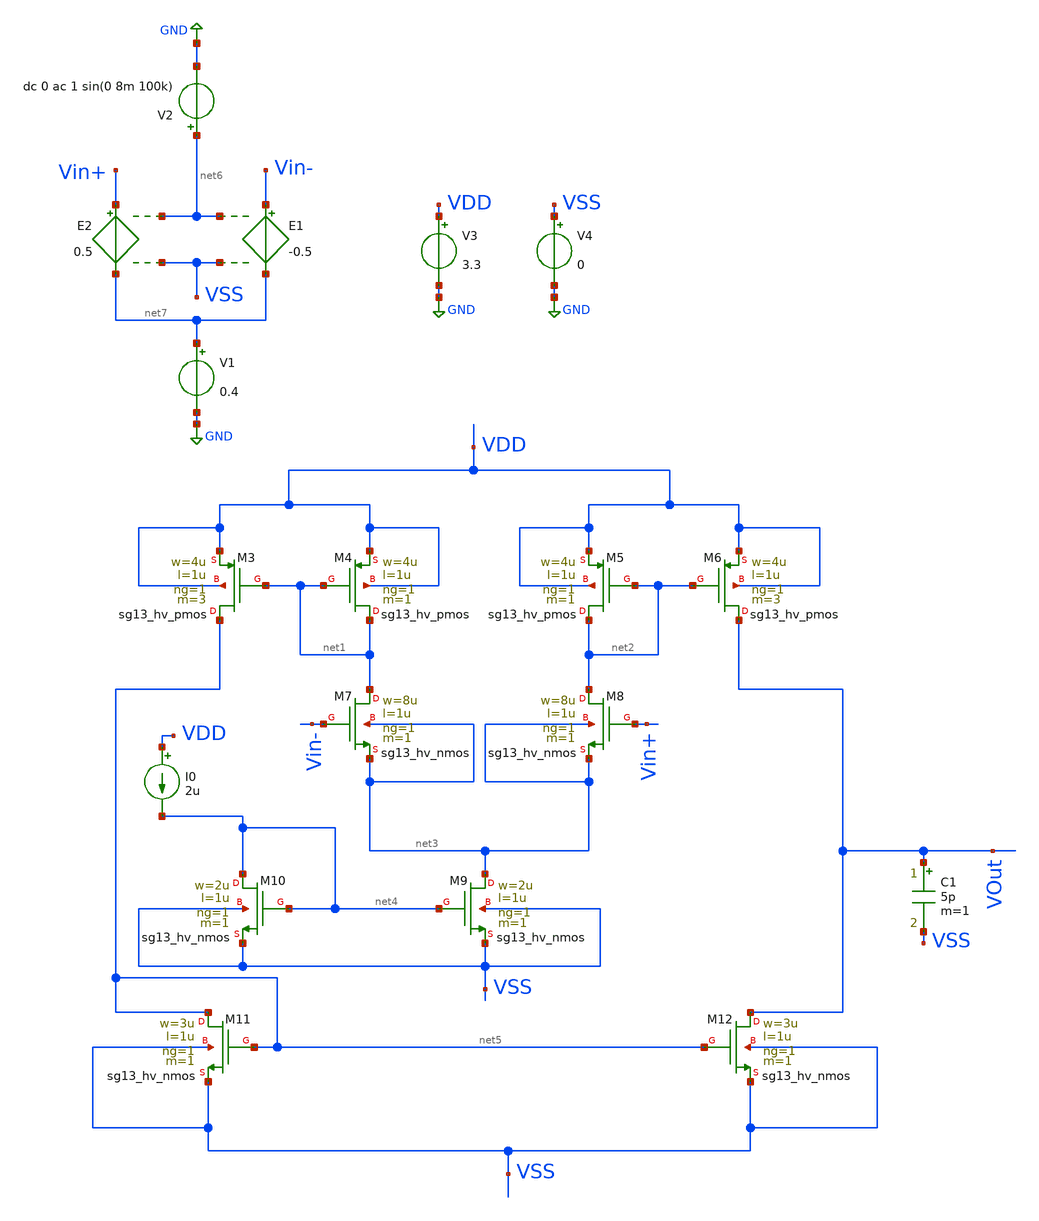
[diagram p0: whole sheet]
** sch_path: BPF/testbench_CurrentM_OTA.sch
**.subckt testbench_CurrentM_OTA
XM3 net5 net1 VDD VDD sg13_hv_pmos w=4u l=1u ng=1 m=3 mm_ok=1
XM5 net2 net2 VDD VDD sg13_hv_pmos w=4u l=1u ng=1 m=1 mm_ok=1
XM6 VOut net2 VDD VDD sg13_hv_pmos w=4u l=1u ng=1 m=3 mm_ok=1
XM7 net1 Vin- net3 net3 sg13_hv_nmos w=8u l=1u ng=1 m=1 mm_ok=1
XM8 net2 Vin+ net3 net3 sg13_hv_nmos w=8u l=1u ng=1 m=1 mm_ok=1
XM9 net3 net4 VSS VSS sg13_hv_nmos w=2u l=1u ng=1 m=1 mm_ok=1
XM10 net4 net4 VSS VSS sg13_hv_nmos w=2u l=1u ng=1 m=1 mm_ok=1
XM11 net5 net5 VSS VSS sg13_hv_nmos w=3u l=1u ng=1 m=1 mm_ok=1
XM12 VOut net5 VSS VSS sg13_hv_nmos w=3u l=1u ng=1 m=1 mm_ok=1
I0 VDD net4 2u
E1 Vin- net7 net6 VSS -0.5
E2 Vin+ net7 net6 VSS 0.5
V1 net7 GND 0.4
V2 net6 GND dc 0 ac 1 sin(0 8m 100k)
V3 VDD GND 3.3
V4 VSS GND 0
C1 VOut VSS 5p m=1
XM4 net1 net1 VDD VDD sg13_hv_pmos w=4u l=1u ng=1 m=1 mm_ok=1
**** begin user architecture code
 .lib cornerMOShv.lib mos_tt


.param temp=27
.save all

.control
  ac dec 80 0.1 11g
  set filetype = ascii
  set units=degrees
  write testbench_CurrentM_OTA.raw vdb(vout) vp(vout)
  set appendwrite
  op
  set filetype = ascii
  write testbench_CurrentM_OTA.raw

  * tran 0.1u 100u
  * set filetype = ascii
  * write testbench_CurrentM_OTA.raw v(vin+) v(vin-) v(vout)
  * set appendwrite
  * op
  * set filetype = ascii
  * write testbench_CurrentM_OTA.raw

.endc


**** end user architecture code
**.ends
.GLOBAL GND
.end
